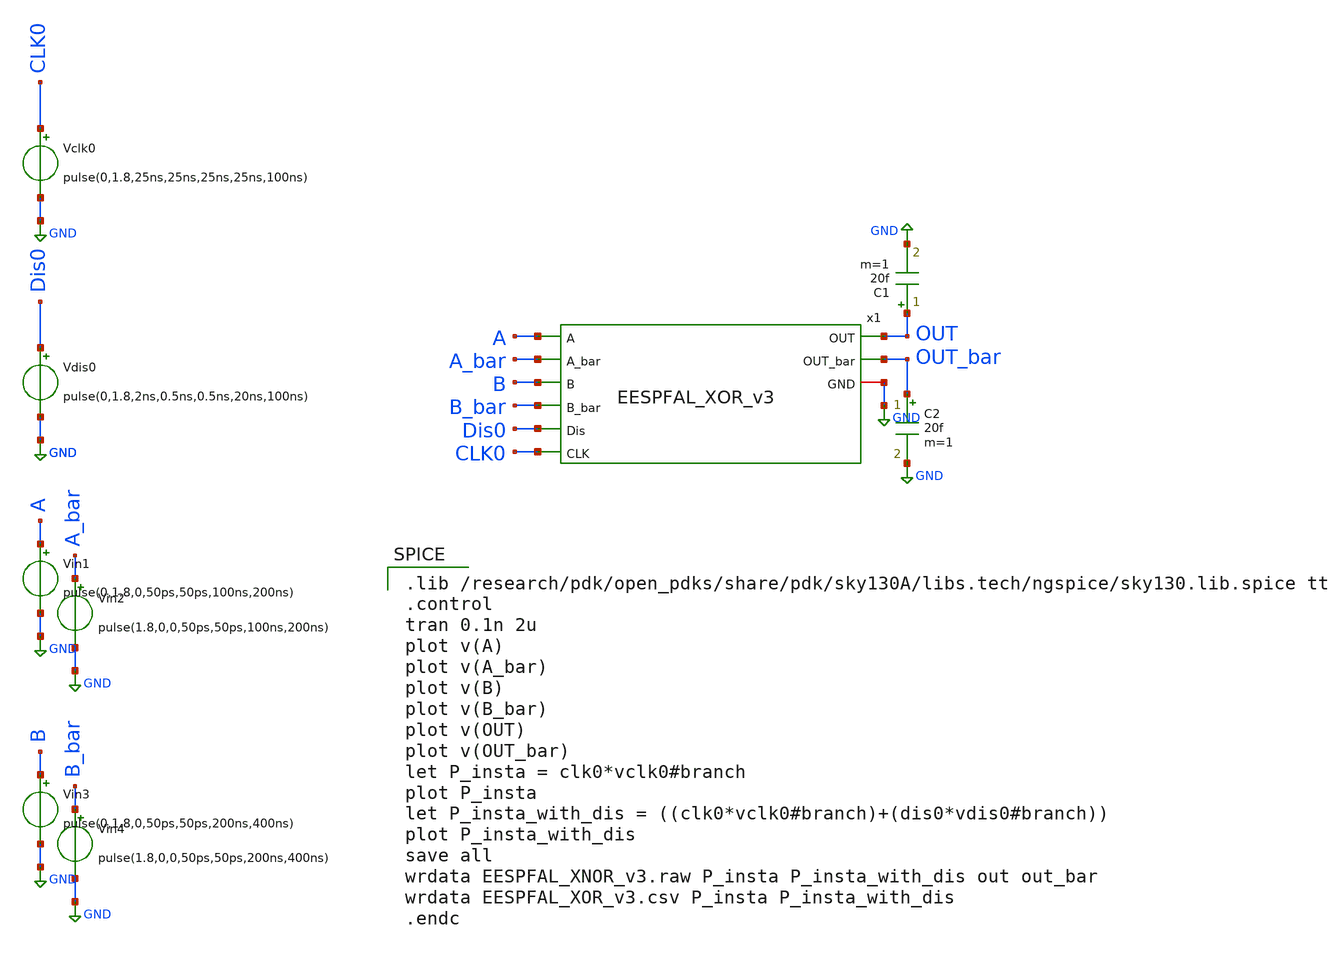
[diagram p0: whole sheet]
** sch_path: skywater_stuff/EESPFAL_XNOR_sim.sch
**.subckt EESPFAL_XNOR_sim
x1 A A_bar B B_bar OUT OUT_bar Dis0 GND CLK0 EESPFAL_XOR_v3
Vin1 A GND pulse(0,1.8,0,50ps,50ps,100ns,200ns)
Vin2 A_bar GND pulse(1.8,0,0,50ps,50ps,100ns,200ns)
Vdis0 Dis0 GND pulse(0,1.8,2ns,0.5ns,0.5ns,20ns,100ns)
Vin3 B GND pulse(0,1.8,0,50ps,50ps,200ns,400ns)
Vin4 B_bar GND pulse(1.8,0,0,50ps,50ps,200ns,400ns)
Vclk0 CLK0 GND pulse(0,1.8,25ns,25ns,25ns,25ns,100ns)
C1 OUT GND 20f m=1
C2 OUT_bar GND 20f m=1
**** begin user architecture code

.lib /research/pdk/open_pdks/share/pdk/sky130A/libs.tech/ngspice/sky130.lib.spice tt
.control
tran 0.1n 2u
plot v(A)
plot v(A_bar)
plot v(B)
plot v(B_bar)
plot v(OUT)
plot v(OUT_bar)
let P_insta = clk0*vclk0#branch
plot P_insta
let P_insta_with_dis = ((clk0*vclk0#branch)+(dis0*vdis0#branch))
plot P_insta_with_dis
save all
wrdata EESPFAL_XNOR_v3.raw P_insta P_insta_with_dis out out_bar
wrdata EESPFAL_XOR_v3.csv P_insta P_insta_with_dis
.endc


**** end user architecture code
**.ends
.GLOBAL GND
.end
